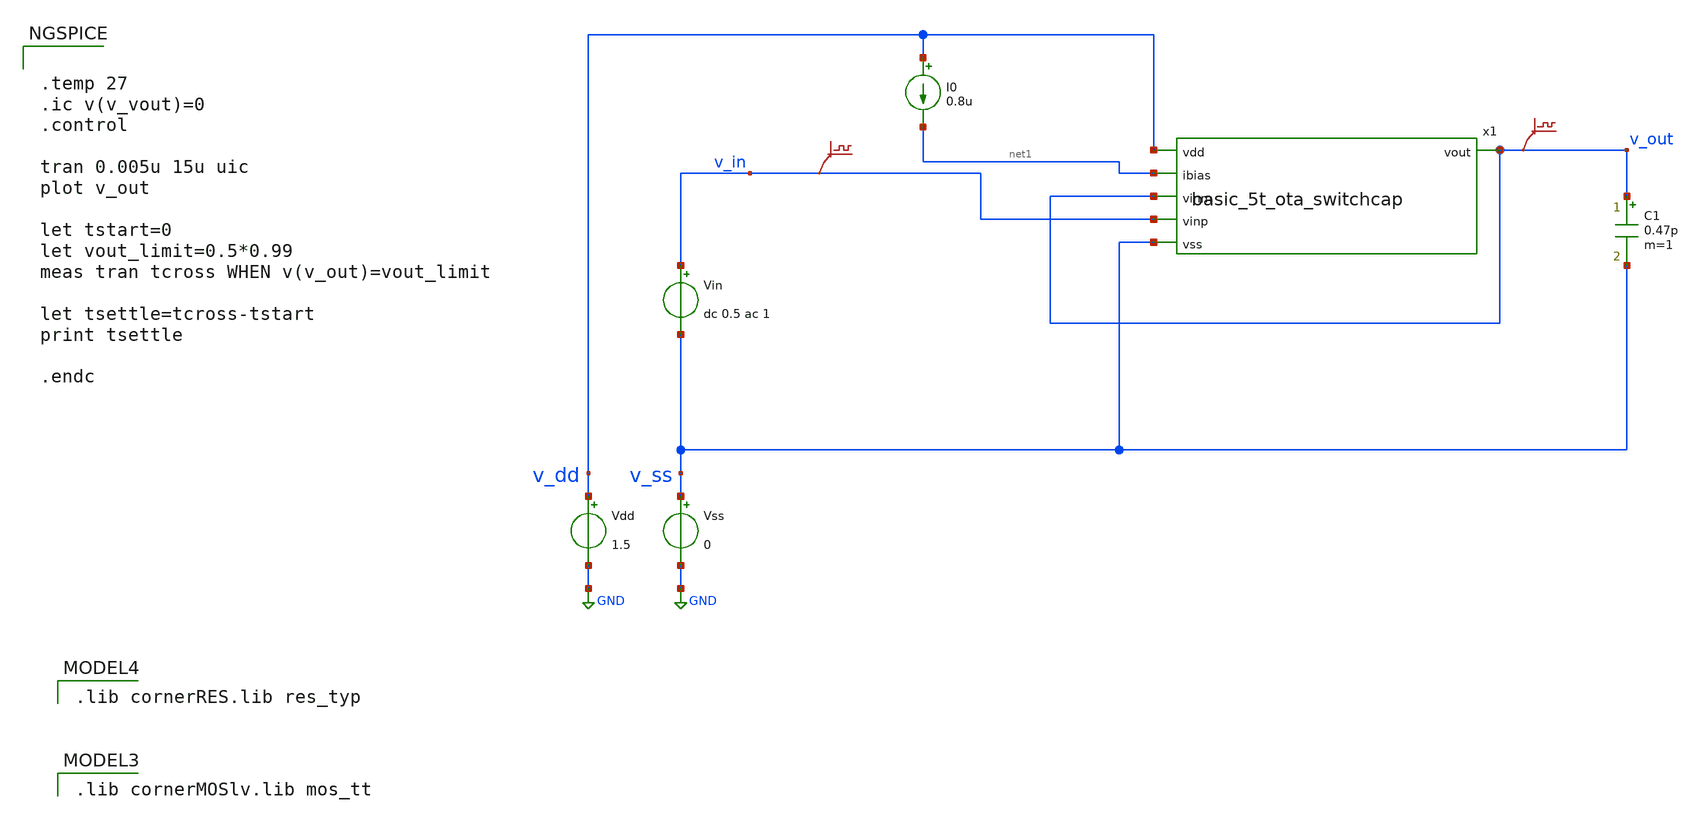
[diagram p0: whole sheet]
** sch_path: design/design_switch_cap/basic_5t_ota_sc_tb_tran.sch
**.subckt basic_5t_ota_sc_tb_tran
Vdd v_dd GND 1.5
Vss v_ss GND 0
C1 v_out v_ss 0.47p m=1
Vin v_in v_ss dc 0.5 ac 1
I0 v_dd net1 0.8u
.save v(v_in)
.save v(v_out)
x1 v_dd v_out net1 v_out v_in v_ss basic_5t_ota_switchcap
**** begin user architecture code
 .lib cornerMOSlv.lib mos_tt

 .lib cornerRES.lib res_typ



.temp 27
.ic v(v_vout)=0
.control

tran 0.005u 15u uic
plot v_out

let tstart=0
let vout_limit=0.5*0.99
meas tran tcross WHEN v(v_out)=vout_limit

let tsettle=tcross-tstart
print tsettle

.endc


**** end user architecture code
**.ends

* expanding   symbol:  basic_5t_ota_switchcap.sym # of pins=6
** sym_path: zip_meiners/ic_design/design_switch_cap/basic_5t_ota_switchcap.sym
** sch_path: zip_meiners/ic_design/design_switch_cap/basic_5t_ota_switchcap.sch
.subckt basic_5t_ota_switchcap vdd vout ibias vinm vinp vss
*.ipin vss
*.ipin vdd
*.ipin ibias
*.ipin vinm
*.ipin vinp
*.opin vout
XM1 vout net1 vdd vdd sg13_lv_pmos w=0.16u l=0.5u ng=1 m=1 mm_ok=1
XM2 vout vinm net2 vss sg13_lv_nmos w=0.15u l=2u ng=1 m=1 mm_ok=1
XM3 net1 net1 vdd vdd sg13_lv_pmos w=0.16u l=0.5u ng=1 m=1 mm_ok=1
XM4 net1 vinp net2 vss sg13_lv_nmos w=0.15u l=2u ng=1 m=1 mm_ok=1
XM5 net2 net3 vss vss sg13_lv_nmos w=0.3u l=2u ng=1 m=1 mm_ok=1
XM6 net4 net3 vss vss sg13_lv_nmos w=0.15u l=2u ng=1 m=1 mm_ok=1
XM7 net3 net3 vss vss sg13_lv_nmos w=0.15u l=2u ng=1 m=1 mm_ok=1
XM9 vdd ibias net4 vss sg13_lv_nmos w=0.15u l=2u ng=1 m=1 mm_ok=1
XM8 ibias ibias net3 vss sg13_lv_nmos w=0.15u l=2u ng=1 m=1 mm_ok=1
.ends

.GLOBAL GND
.end
